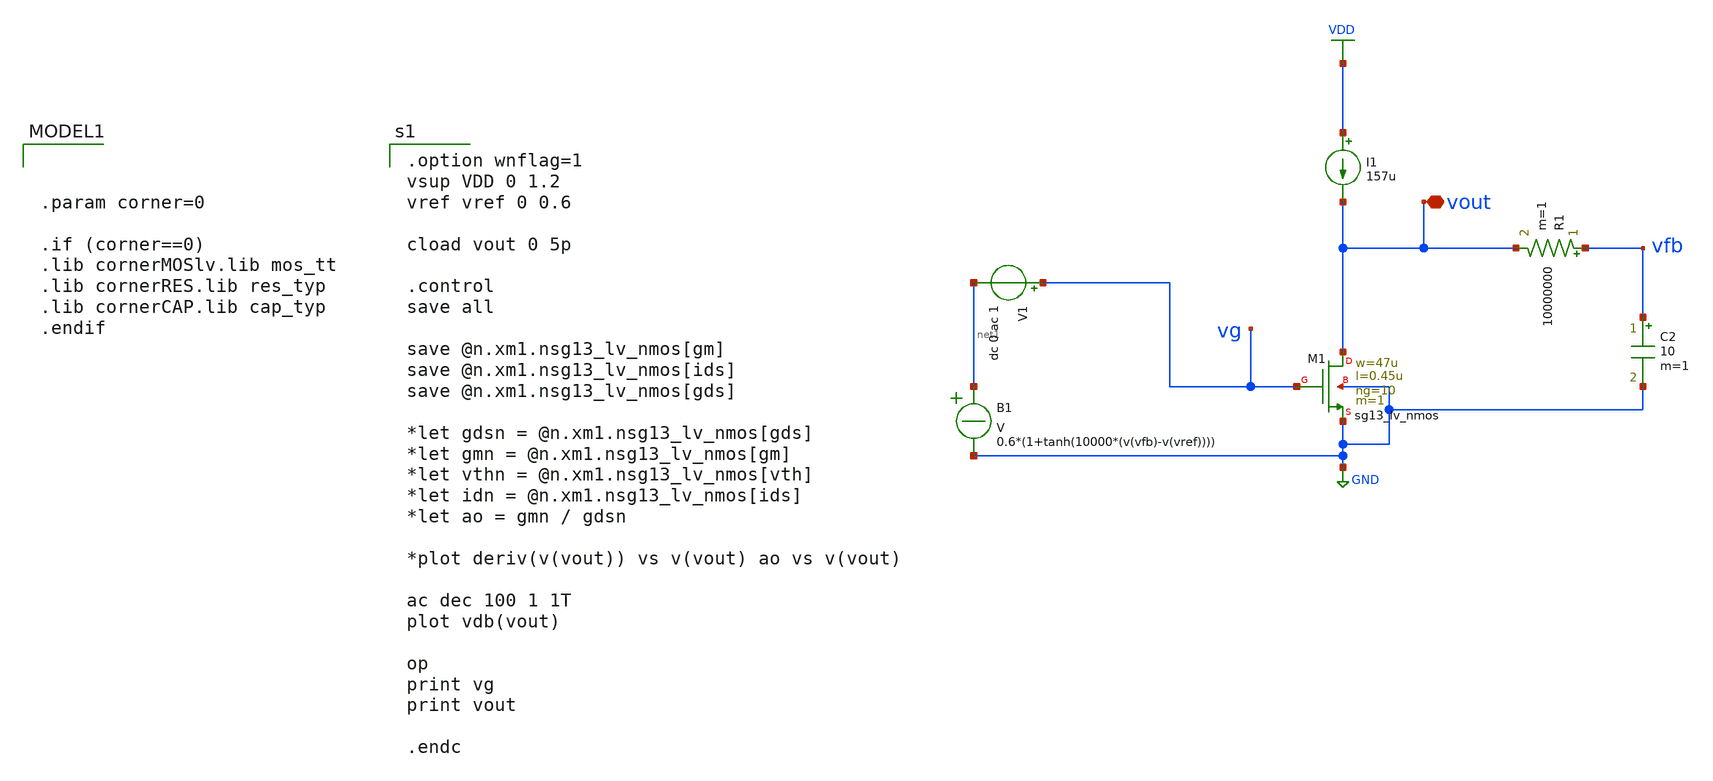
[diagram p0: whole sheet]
** sch_path: xschem/Tareas/Tarea_1/cs_amp_full_FIXED_MIE955HW1.sch
**.subckt cs_amp_full_FIXED_MIE955HW1 vout
*.iopin vout
I1 VDD vout 157u
XM1 vout vg GND GND sg13_lv_nmos w=47u l=0.45u ng=10 m=1 mm_ok=1
B1 net1 GND V = 0.6*(1+tanh(10000*(v(vfb)-v(vref))))
V1 vg net1 dc 0 ac 1
R1 vfb vout 10000000 m=1
C2 vfb GND 10 m=1
**** begin user architecture code

.option wnflag=1
vsup VDD 0 1.2
vref vref 0 0.6

cload vout 0 5p

.control
save all

save @n.xm1.nsg13_lv_nmos[gm]
save @n.xm1.nsg13_lv_nmos[ids]
save @n.xm1.nsg13_lv_nmos[gds]

*let gdsn = @n.xm1.nsg13_lv_nmos[gds]
*let gmn = @n.xm1.nsg13_lv_nmos[gm]
*let vthn = @n.xm1.nsg13_lv_nmos[vth]
*let idn = @n.xm1.nsg13_lv_nmos[ids]
*let ao = gmn / gdsn

*plot deriv(v(vout)) vs v(vout) ao vs v(vout)

ac dec 100 1 1T
plot vdb(vout)

op
print vg
print vout

.endc



.param corner=0

.if (corner==0)
.lib cornerMOSlv.lib mos_tt
.lib cornerRES.lib res_typ
.lib cornerCAP.lib cap_typ
.endif

**** end user architecture code
**.ends
.GLOBAL GND
.GLOBAL VDD
.end
